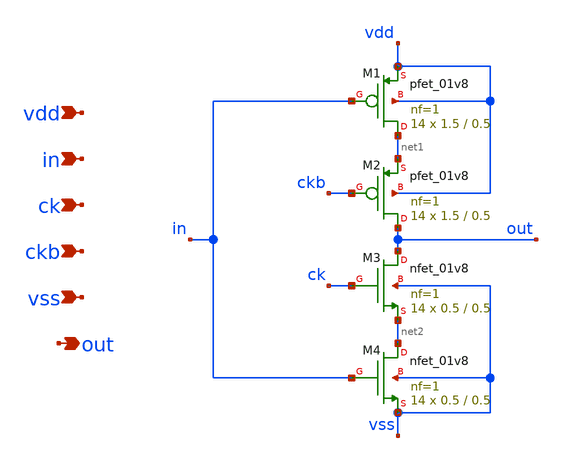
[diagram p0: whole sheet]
** sch_path: xschem/dac_sw_4.sch
**.subckt dac_sw_4 vdd in ck ckb vss out
*.ipin vdd
*.ipin in
*.ipin ck
*.ipin ckb
*.ipin vss
*.opin out
XM1 net1 in vdd vdd sky130_fd_pr__pfet_01v8 L=0.5 W=1.5 nf=1 ad='int((nf+1)/2) * W/nf * 0.29' as='int((nf+2)/2) * W/nf * 0.29'
+ pd='2*int((nf+1)/2) * (W/nf + 0.29)' ps='2*int((nf+2)/2) * (W/nf + 0.29)' nrd='0.29 / W' nrs='0.29 / W'
+ sa=0 sb=0 sd=0 mult=14 m=14
XM2 out ckb net1 vdd sky130_fd_pr__pfet_01v8 L=0.5 W=1.5 nf=1 ad='int((nf+1)/2) * W/nf * 0.29' as='int((nf+2)/2) * W/nf * 0.29'
+ pd='2*int((nf+1)/2) * (W/nf + 0.29)' ps='2*int((nf+2)/2) * (W/nf + 0.29)' nrd='0.29 / W' nrs='0.29 / W'
+ sa=0 sb=0 sd=0 mult=14 m=14
XM3 out ck net2 vss sky130_fd_pr__nfet_01v8 L=0.5 W=0.5 nf=1 ad='int((nf+1)/2) * W/nf * 0.29' as='int((nf+2)/2) * W/nf * 0.29'
+ pd='2*int((nf+1)/2) * (W/nf + 0.29)' ps='2*int((nf+2)/2) * (W/nf + 0.29)' nrd='0.29 / W' nrs='0.29 / W'
+ sa=0 sb=0 sd=0 mult=14 m=14
XM4 net2 in vss vss sky130_fd_pr__nfet_01v8 L=0.5 W=0.5 nf=1 ad='int((nf+1)/2) * W/nf * 0.29' as='int((nf+2)/2) * W/nf * 0.29'
+ pd='2*int((nf+1)/2) * (W/nf + 0.29)' ps='2*int((nf+2)/2) * (W/nf + 0.29)' nrd='0.29 / W' nrs='0.29 / W'
+ sa=0 sb=0 sd=0 mult=14 m=14
**.ends
.end
